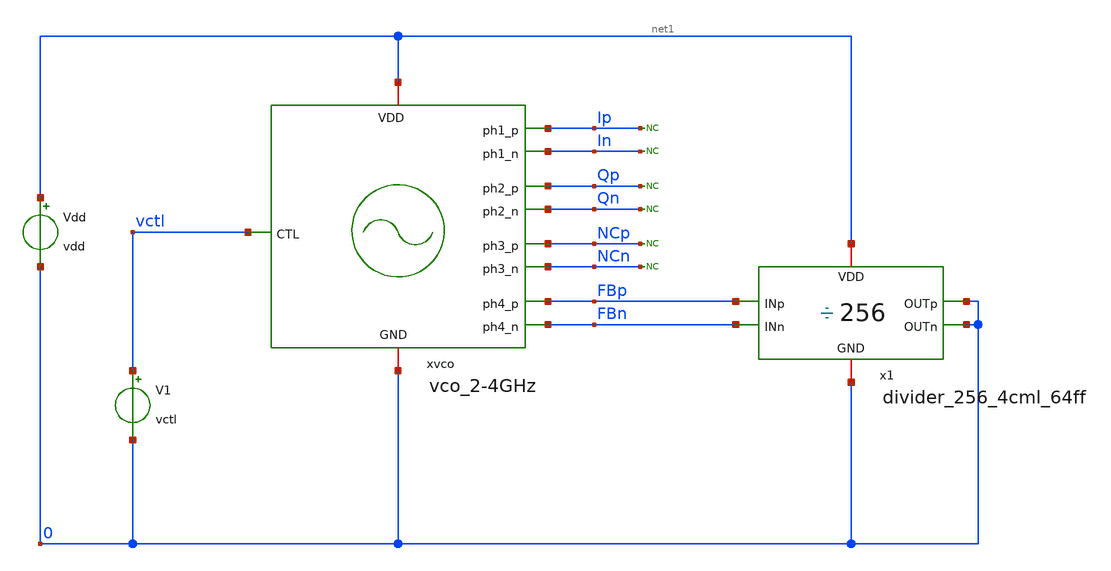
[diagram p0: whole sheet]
** sch_path: design/vco_2-4GHz/tests/vco_2-4GHz_tb.sch
**.subckt vco_2-4GHz_tb
V1 vctl 0 vctl
Vdd net1 0 vdd
x1 net1 0 FBp FBn 0 0 divider_256_4cml_64ff
* noconn Qp
* noconn Qn
xvco net1 Ip In Qp Qn NCp NCn FBp FBn vctl 0 vco_2-4GHz
* noconn Ip
* noconn In
* noconn NCp
* noconn NCn
**** begin user architecture code


.param temp=-40
.temp -40

.lib sky130_fd_pr/models/sky130.lib.spice tt
.tran 0.001n 10n uic
.param vdd=1.8
.param vctl=0.0


**** end user architecture code
**.ends
.end
